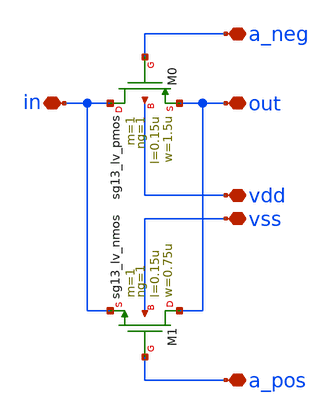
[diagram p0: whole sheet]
** sch_path: design/blocks/transmissiongate/schematic/transmissiongate.sch
**.subckt transmissiongate vdd vss out in a_neg a_pos
*.iopin vdd
*.iopin vss
*.iopin out
*.iopin in
*.iopin a_neg
*.iopin a_pos
XM0 in a_neg out vdd sg13_lv_pmos w=1.5u l=0.15u ng=1 m=1 mm_ok=1
XM1 out a_pos in vss sg13_lv_nmos w=0.75u l=0.15u ng=1 m=1 mm_ok=1
**.ends
.end
